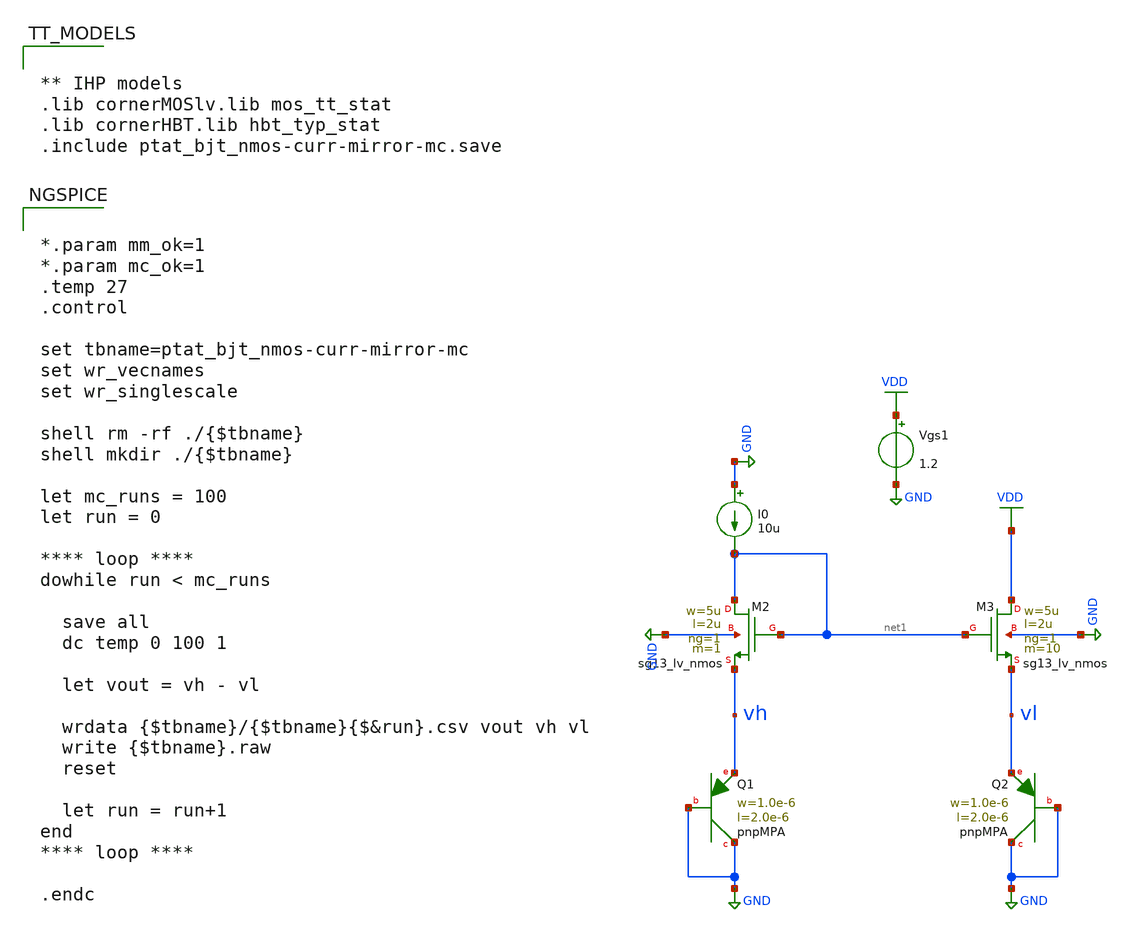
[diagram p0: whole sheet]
** sch_path: TempSensor/design_data/xschem/ptat_bjt_nmos-curr-mirror-mc.sch
**.subckt ptat_bjt_nmos-curr-mirror-mc
XM2 net1 net1 vh GND sg13_lv_nmos w=5u l=2u ng=1 m=1 mm_ok=1
XM3 VDD net1 vl GND sg13_lv_nmos w=5u l=2u ng=1 m=10 mm_ok=1
I0 GND net1 10u
Vgs1 VDD GND 1.2
XQ2 GND GND vl pnpMPA a=2p p=6u m=1
XQ1 GND GND vh pnpMPA a=2p p=6u m=1
**** begin user architecture code


*.param mm_ok=1
*.param mc_ok=1
.temp 27
.control

set tbname=ptat_bjt_nmos-curr-mirror-mc
set wr_vecnames
set wr_singlescale

shell rm -rf ./{$tbname}
shell mkdir ./{$tbname}

let mc_runs = 100
let run = 0

**** loop ****
dowhile run < mc_runs

  save all
  dc temp 0 100 1

  let vout = vh - vl

  wrdata {$tbname}/{$tbname}{$&run}.csv vout vh vl
  write {$tbname}.raw
  reset

  let run = run+1
end
**** loop ****

.endc




** IHP models
.lib cornerMOSlv.lib mos_tt_stat
.lib cornerHBT.lib hbt_typ_stat
.include ptat_bjt_nmos-curr-mirror-mc.save


**** end user architecture code
**.ends
.GLOBAL GND
.GLOBAL VDD
.end
